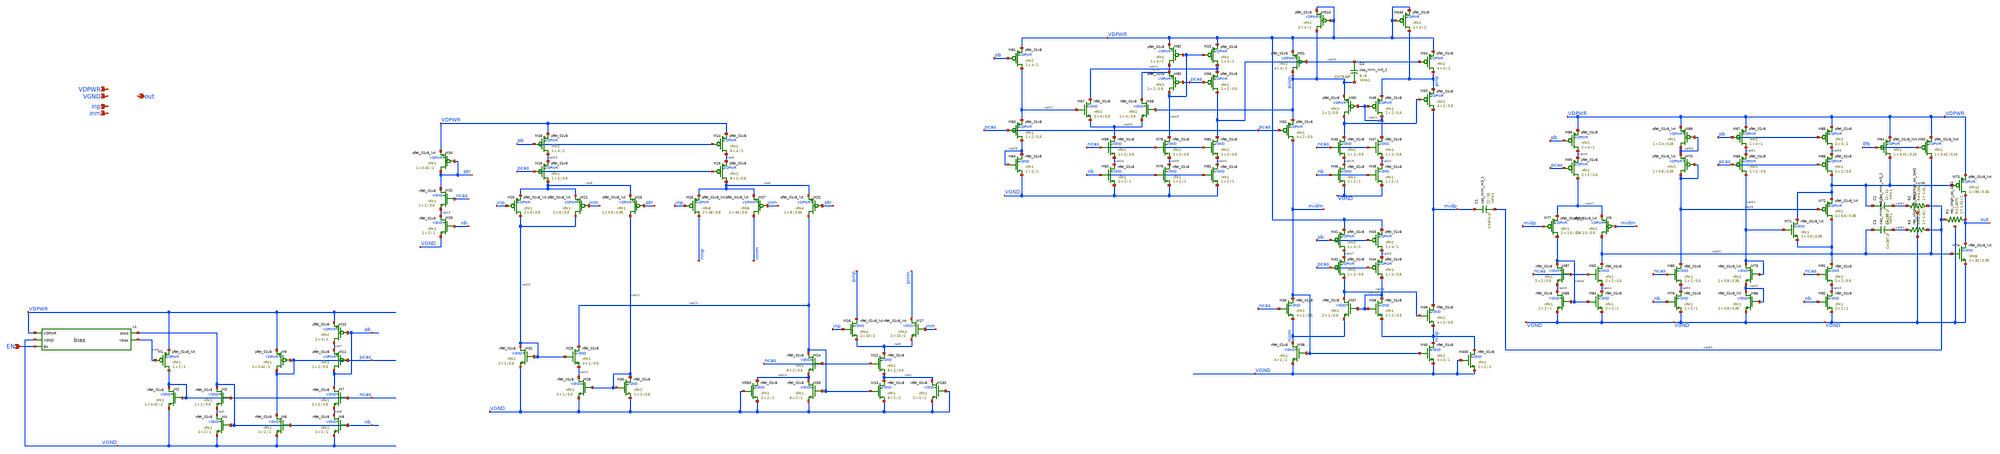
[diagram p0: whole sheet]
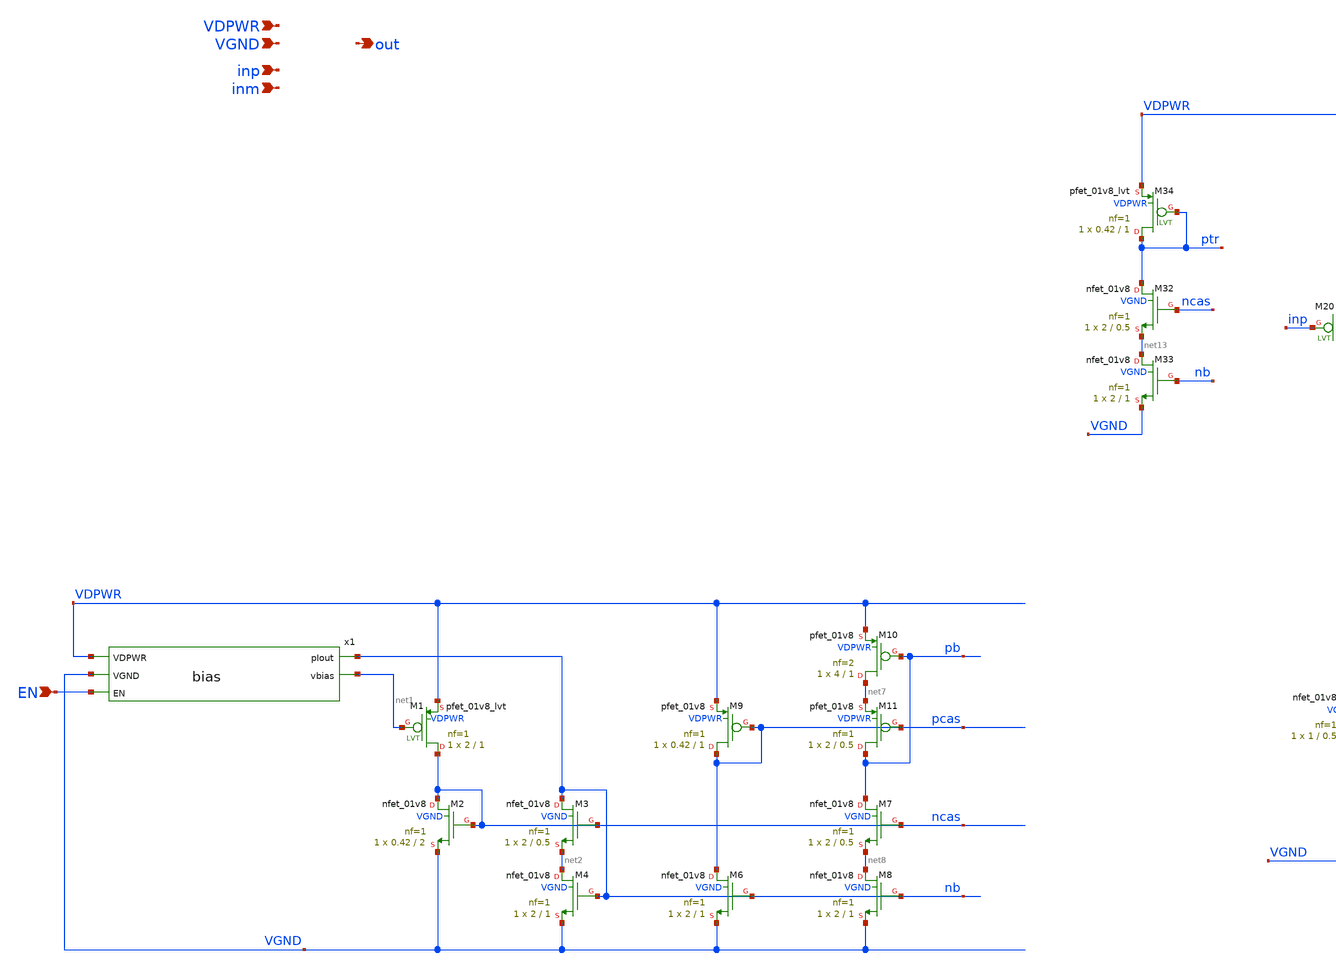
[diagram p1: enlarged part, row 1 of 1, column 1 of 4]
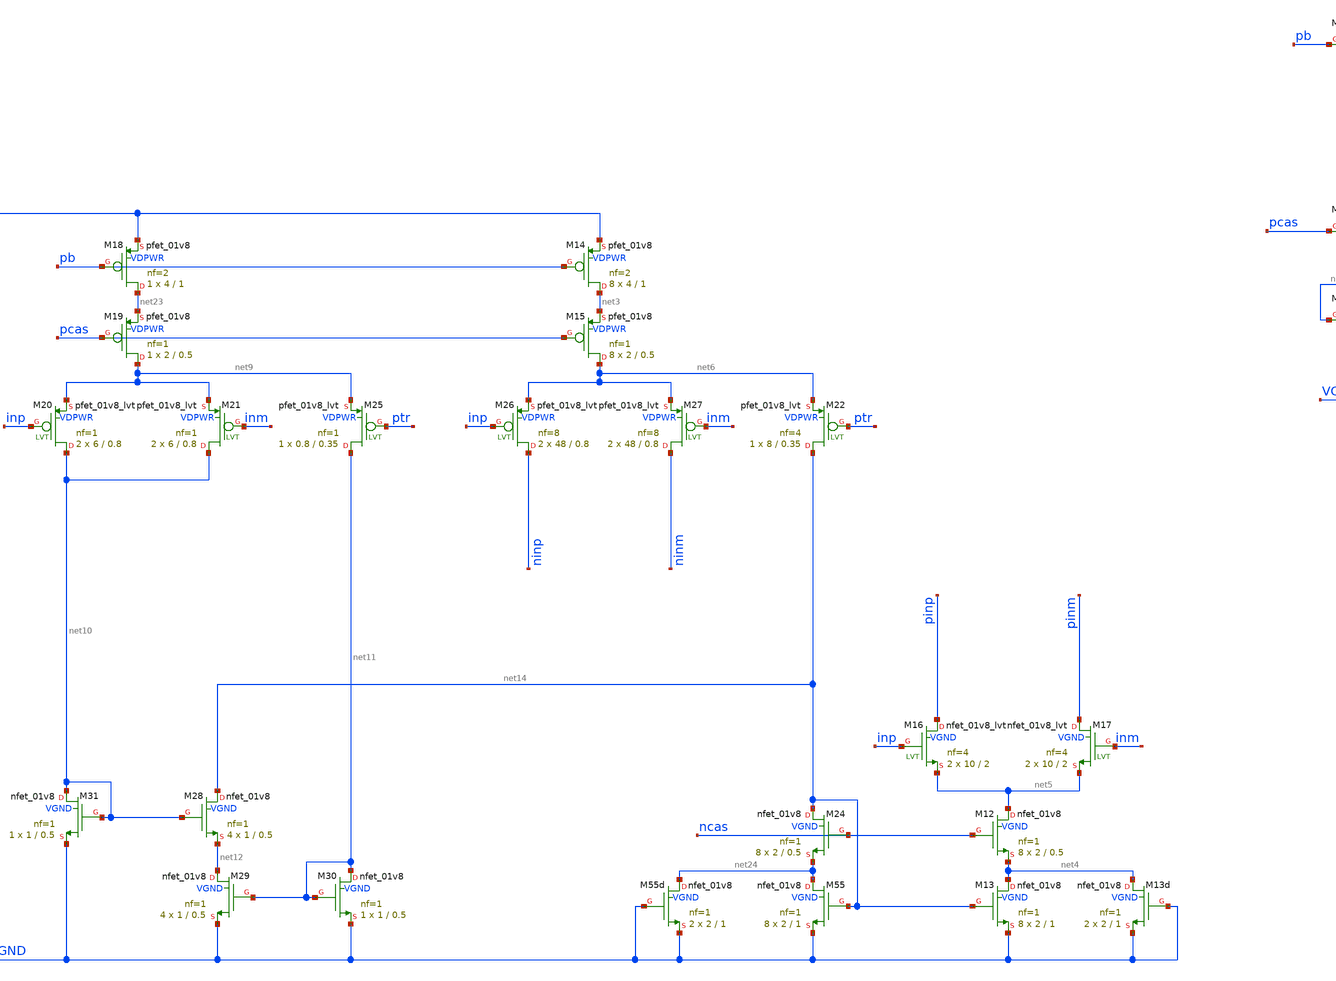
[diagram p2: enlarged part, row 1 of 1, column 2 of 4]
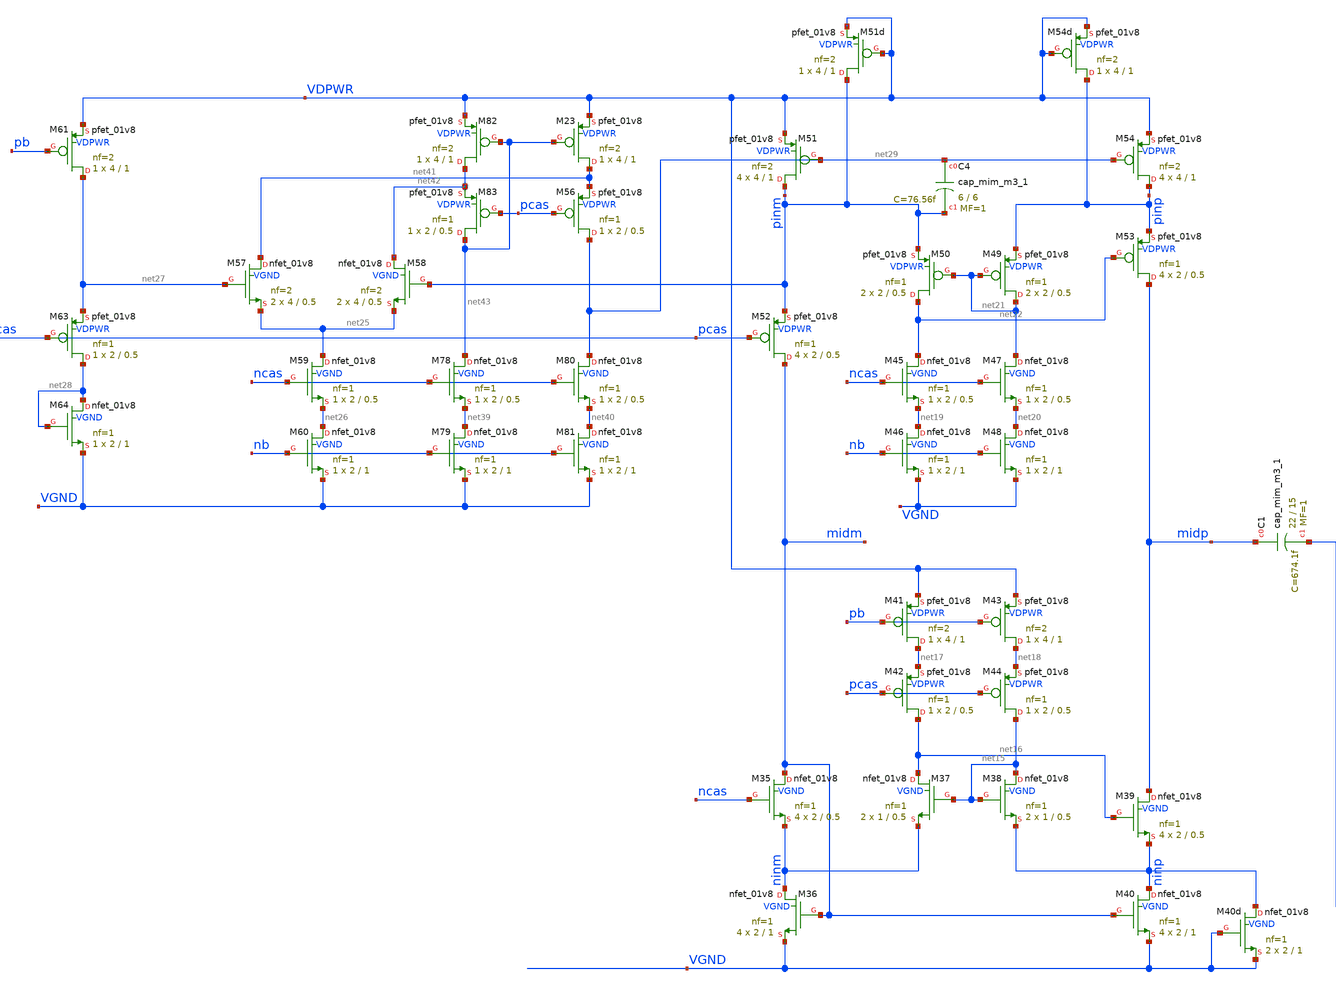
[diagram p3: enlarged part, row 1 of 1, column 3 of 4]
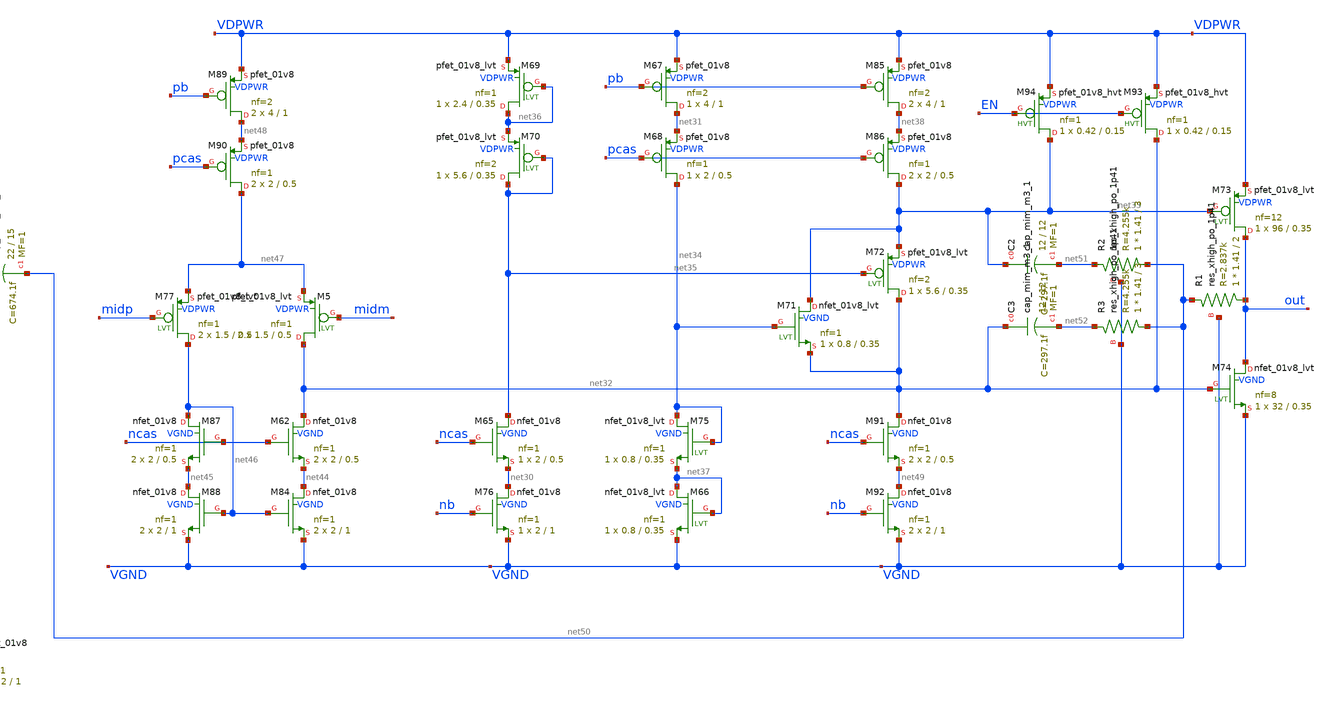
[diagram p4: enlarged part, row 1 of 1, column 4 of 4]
** sch_path: xschem/opamp.sch
**.subckt opamp VDPWR VGND inp inm out EN
*.ipin VDPWR
*.ipin VGND
*.ipin inp
*.ipin inm
*.opin out
*.ipin EN
x1 VDPWR nb VGND EN net1 bias
XM1 ncas net1 VDPWR VDPWR sky130_fd_pr__pfet_01v8_lvt L=1 W=2 nf=1 ad='int((1 + 1)/2) * 2 / 1 * 0.29'
+ as='int((1 + 2)/2) * 2 / 1 * 0.29' pd='2*int((1 + 1)/2) * (2 / 1 + 0.29)' ps='2*int((1 + 2)/2) * (2 / 1 + 0.29)'
+ nrd='0.29 / 2 ' nrs='0.29 / 2 ' sa=0 sb=0 sd=0 mult=1 m=1
XM2 ncas ncas VGND VGND sky130_fd_pr__nfet_01v8 L=2 W=0.42 nf=1 ad='int((1 + 1)/2) * 0.42 / 1 * 0.29'
+ as='int((1 + 2)/2) * 0.42 / 1 * 0.29' pd='2*int((1 + 1)/2) * (0.42 / 1 + 0.29)' ps='2*int((1 + 2)/2) * (0.42 / 1 + 0.29)'
+ nrd='0.29 / 0.42 ' nrs='0.29 / 0.42 ' sa=0 sb=0 sd=0 mult=1 m=1
XM3 nb ncas net2 VGND sky130_fd_pr__nfet_01v8 L=0.5 W=2 nf=1 ad='int((1 + 1)/2) * 2 / 1 * 0.29' as='int((1 + 2)/2) * 2 / 1 * 0.29'
+ pd='2*int((1 + 1)/2) * (2 / 1 + 0.29)' ps='2*int((1 + 2)/2) * (2 / 1 + 0.29)' nrd='0.29 / 2 ' nrs='0.29 / 2 '
+ sa=0 sb=0 sd=0 mult=1 m=1
XM4 net2 nb VGND VGND sky130_fd_pr__nfet_01v8 L=1 W=2 nf=1 ad='int((1 + 1)/2) * 2 / 1 * 0.29' as='int((1 + 2)/2) * 2 / 1 * 0.29'
+ pd='2*int((1 + 1)/2) * (2 / 1 + 0.29)' ps='2*int((1 + 2)/2) * (2 / 1 + 0.29)' nrd='0.29 / 2 ' nrs='0.29 / 2 '
+ sa=0 sb=0 sd=0 mult=1 m=1
XM6 pcas nb VGND VGND sky130_fd_pr__nfet_01v8 L=1 W=2 nf=1 ad='int((1 + 1)/2) * 2 / 1 * 0.29' as='int((1 + 2)/2) * 2 / 1 * 0.29'
+ pd='2*int((1 + 1)/2) * (2 / 1 + 0.29)' ps='2*int((1 + 2)/2) * (2 / 1 + 0.29)' nrd='0.29 / 2 ' nrs='0.29 / 2 '
+ sa=0 sb=0 sd=0 mult=1 m=1
XM7 pb ncas net8 VGND sky130_fd_pr__nfet_01v8 L=0.5 W=2 nf=1 ad='int((1 + 1)/2) * 2 / 1 * 0.29' as='int((1 + 2)/2) * 2 / 1 * 0.29'
+ pd='2*int((1 + 1)/2) * (2 / 1 + 0.29)' ps='2*int((1 + 2)/2) * (2 / 1 + 0.29)' nrd='0.29 / 2 ' nrs='0.29 / 2 '
+ sa=0 sb=0 sd=0 mult=1 m=1
XM8 net8 nb VGND VGND sky130_fd_pr__nfet_01v8 L=1 W=2 nf=1 ad='int((1 + 1)/2) * 2 / 1 * 0.29' as='int((1 + 2)/2) * 2 / 1 * 0.29'
+ pd='2*int((1 + 1)/2) * (2 / 1 + 0.29)' ps='2*int((1 + 2)/2) * (2 / 1 + 0.29)' nrd='0.29 / 2 ' nrs='0.29 / 2 '
+ sa=0 sb=0 sd=0 mult=1 m=1
XM9 pcas pcas VDPWR VDPWR sky130_fd_pr__pfet_01v8 L=1 W=0.42 nf=1 ad='int((1 + 1)/2) * 0.42 / 1 * 0.29'
+ as='int((1 + 2)/2) * 0.42 / 1 * 0.29' pd='2*int((1 + 1)/2) * (0.42 / 1 + 0.29)' ps='2*int((1 + 2)/2) * (0.42 / 1 + 0.29)'
+ nrd='0.29 / 0.42 ' nrs='0.29 / 0.42 ' sa=0 sb=0 sd=0 mult=1 m=1
XM10 net7 pb VDPWR VDPWR sky130_fd_pr__pfet_01v8 L=1 W=4 nf=2 ad='int((2 + 1)/2) * 4 / 2 * 0.29' as='int((2 + 2)/2) * 4 / 2 * 0.29'
+ pd='2*int((2 + 1)/2) * (4 / 2 + 0.29)' ps='2*int((2 + 2)/2) * (4 / 2 + 0.29)' nrd='0.29 / 4 ' nrs='0.29 / 4 '
+ sa=0 sb=0 sd=0 mult=1 m=1
XM11 pb pcas net7 VDPWR sky130_fd_pr__pfet_01v8 L=0.5 W=2 nf=1 ad='int((1 + 1)/2) * 2 / 1 * 0.29' as='int((1 + 2)/2) * 2 / 1 * 0.29'
+ pd='2*int((1 + 1)/2) * (2 / 1 + 0.29)' ps='2*int((1 + 2)/2) * (2 / 1 + 0.29)' nrd='0.29 / 2 ' nrs='0.29 / 2 '
+ sa=0 sb=0 sd=0 mult=1 m=1
XM12 net5 ncas net4 VGND sky130_fd_pr__nfet_01v8 L=0.5 W=2 nf=1 ad='int((1 + 1)/2) * 2 / 1 * 0.29' as='int((1 + 2)/2) * 2 / 1 * 0.29'
+ pd='2*int((1 + 1)/2) * (2 / 1 + 0.29)' ps='2*int((1 + 2)/2) * (2 / 1 + 0.29)' nrd='0.29 / 2 ' nrs='0.29 / 2 '
+ sa=0 sb=0 sd=0 mult=8 m=8
XM13 net4 net14 VGND VGND sky130_fd_pr__nfet_01v8 L=1 W=2 nf=1 ad='int((1 + 1)/2) * 2 / 1 * 0.29' as='int((1 + 2)/2) * 2 / 1 * 0.29'
+ pd='2*int((1 + 1)/2) * (2 / 1 + 0.29)' ps='2*int((1 + 2)/2) * (2 / 1 + 0.29)' nrd='0.29 / 2 ' nrs='0.29 / 2 '
+ sa=0 sb=0 sd=0 mult=8 m=8
XM14 net3 pb VDPWR VDPWR sky130_fd_pr__pfet_01v8 L=1 W=4 nf=2 ad='int((2 + 1)/2) * 4 / 2 * 0.29' as='int((2 + 2)/2) * 4 / 2 * 0.29'
+ pd='2*int((2 + 1)/2) * (4 / 2 + 0.29)' ps='2*int((2 + 2)/2) * (4 / 2 + 0.29)' nrd='0.29 / 4 ' nrs='0.29 / 4 '
+ sa=0 sb=0 sd=0 mult=8 m=8
XM15 net6 pcas net3 VDPWR sky130_fd_pr__pfet_01v8 L=0.5 W=2 nf=1 ad='int((1 + 1)/2) * 2 / 1 * 0.29' as='int((1 + 2)/2) * 2 / 1 * 0.29'
+ pd='2*int((1 + 1)/2) * (2 / 1 + 0.29)' ps='2*int((1 + 2)/2) * (2 / 1 + 0.29)' nrd='0.29 / 2 ' nrs='0.29 / 2 '
+ sa=0 sb=0 sd=0 mult=8 m=8
XM16 pinp inp net5 VGND sky130_fd_pr__nfet_01v8_lvt L=2 W=10 nf=4 ad='int((4 + 1)/2) * 10 / 4 * 0.29'
+ as='int((4 + 2)/2) * 10 / 4 * 0.29' pd='2*int((4 + 1)/2) * (10 / 4 + 0.29)' ps='2*int((4 + 2)/2) * (10 / 4 + 0.29)'
+ nrd='0.29 / 10 ' nrs='0.29 / 10 ' sa=0 sb=0 sd=0 mult=2 m=2
XM17 pinm inm net5 VGND sky130_fd_pr__nfet_01v8_lvt L=2 W=10 nf=4 ad='int((4 + 1)/2) * 10 / 4 * 0.29'
+ as='int((4 + 2)/2) * 10 / 4 * 0.29' pd='2*int((4 + 1)/2) * (10 / 4 + 0.29)' ps='2*int((4 + 2)/2) * (10 / 4 + 0.29)'
+ nrd='0.29 / 10 ' nrs='0.29 / 10 ' sa=0 sb=0 sd=0 mult=2 m=2
XM26 ninp inp net6 VDPWR sky130_fd_pr__pfet_01v8_lvt L=0.8 W=48 nf=8 ad='int((8 + 1)/2) * 48 / 8 * 0.29'
+ as='int((8 + 2)/2) * 48 / 8 * 0.29' pd='2*int((8 + 1)/2) * (48 / 8 + 0.29)' ps='2*int((8 + 2)/2) * (48 / 8 + 0.29)'
+ nrd='0.29 / 48 ' nrs='0.29 / 48 ' sa=0 sb=0 sd=0 mult=2 m=2
XM27 ninm inm net6 VDPWR sky130_fd_pr__pfet_01v8_lvt L=0.8 W=48 nf=8 ad='int((8 + 1)/2) * 48 / 8 * 0.29'
+ as='int((8 + 2)/2) * 48 / 8 * 0.29' pd='2*int((8 + 1)/2) * (48 / 8 + 0.29)' ps='2*int((8 + 2)/2) * (48 / 8 + 0.29)'
+ nrd='0.29 / 48 ' nrs='0.29 / 48 ' sa=0 sb=0 sd=0 mult=2 m=2
XM18 net23 pb VDPWR VDPWR sky130_fd_pr__pfet_01v8 L=1 W=4 nf=2 ad='int((2 + 1)/2) * 4 / 2 * 0.29' as='int((2 + 2)/2) * 4 / 2 * 0.29'
+ pd='2*int((2 + 1)/2) * (4 / 2 + 0.29)' ps='2*int((2 + 2)/2) * (4 / 2 + 0.29)' nrd='0.29 / 4 ' nrs='0.29 / 4 '
+ sa=0 sb=0 sd=0 mult=1 m=1
XM19 net9 pcas net23 VDPWR sky130_fd_pr__pfet_01v8 L=0.5 W=2 nf=1 ad='int((1 + 1)/2) * 2 / 1 * 0.29'
+ as='int((1 + 2)/2) * 2 / 1 * 0.29' pd='2*int((1 + 1)/2) * (2 / 1 + 0.29)' ps='2*int((1 + 2)/2) * (2 / 1 + 0.29)'
+ nrd='0.29 / 2 ' nrs='0.29 / 2 ' sa=0 sb=0 sd=0 mult=1 m=1
XM20 net10 inp net9 VDPWR sky130_fd_pr__pfet_01v8_lvt L=0.8 W=6 nf=1 ad='int((1 + 1)/2) * 6 / 1 * 0.29'
+ as='int((1 + 2)/2) * 6 / 1 * 0.29' pd='2*int((1 + 1)/2) * (6 / 1 + 0.29)' ps='2*int((1 + 2)/2) * (6 / 1 + 0.29)'
+ nrd='0.29 / 6 ' nrs='0.29 / 6 ' sa=0 sb=0 sd=0 mult=2 m=2
XM21 net10 inm net9 VDPWR sky130_fd_pr__pfet_01v8_lvt L=0.8 W=6 nf=1 ad='int((1 + 1)/2) * 6 / 1 * 0.29'
+ as='int((1 + 2)/2) * 6 / 1 * 0.29' pd='2*int((1 + 1)/2) * (6 / 1 + 0.29)' ps='2*int((1 + 2)/2) * (6 / 1 + 0.29)'
+ nrd='0.29 / 6 ' nrs='0.29 / 6 ' sa=0 sb=0 sd=0 mult=2 m=2
XM25 net11 ptr net9 VDPWR sky130_fd_pr__pfet_01v8_lvt L=0.35 W=0.8 nf=1 ad='int((1 + 1)/2) * 0.8 / 1 * 0.29'
+ as='int((1 + 2)/2) * 0.8 / 1 * 0.29' pd='2*int((1 + 1)/2) * (0.8 / 1 + 0.29)' ps='2*int((1 + 2)/2) * (0.8 / 1 + 0.29)'
+ nrd='0.29 / 0.8 ' nrs='0.29 / 0.8 ' sa=0 sb=0 sd=0 mult=1 m=1
XM28 net14 net10 net12 VGND sky130_fd_pr__nfet_01v8 L=0.5 W=1 nf=1 ad='int((1 + 1)/2) * 1 / 1 * 0.29'
+ as='int((1 + 2)/2) * 1 / 1 * 0.29' pd='2*int((1 + 1)/2) * (1 / 1 + 0.29)' ps='2*int((1 + 2)/2) * (1 / 1 + 0.29)'
+ nrd='0.29 / 1 ' nrs='0.29 / 1 ' sa=0 sb=0 sd=0 mult=4 m=4
XM29 net12 net11 VGND VGND sky130_fd_pr__nfet_01v8 L=0.5 W=1 nf=1 ad='int((1 + 1)/2) * 1 / 1 * 0.29'
+ as='int((1 + 2)/2) * 1 / 1 * 0.29' pd='2*int((1 + 1)/2) * (1 / 1 + 0.29)' ps='2*int((1 + 2)/2) * (1 / 1 + 0.29)'
+ nrd='0.29 / 1 ' nrs='0.29 / 1 ' sa=0 sb=0 sd=0 mult=4 m=4
XM30 net11 net11 VGND VGND sky130_fd_pr__nfet_01v8 L=0.5 W=1 nf=1 ad='int((1 + 1)/2) * 1 / 1 * 0.29'
+ as='int((1 + 2)/2) * 1 / 1 * 0.29' pd='2*int((1 + 1)/2) * (1 / 1 + 0.29)' ps='2*int((1 + 2)/2) * (1 / 1 + 0.29)'
+ nrd='0.29 / 1 ' nrs='0.29 / 1 ' sa=0 sb=0 sd=0 mult=1 m=1
XM31 net10 net10 VGND VGND sky130_fd_pr__nfet_01v8 L=0.5 W=1 nf=1 ad='int((1 + 1)/2) * 1 / 1 * 0.29'
+ as='int((1 + 2)/2) * 1 / 1 * 0.29' pd='2*int((1 + 1)/2) * (1 / 1 + 0.29)' ps='2*int((1 + 2)/2) * (1 / 1 + 0.29)'
+ nrd='0.29 / 1 ' nrs='0.29 / 1 ' sa=0 sb=0 sd=0 mult=1 m=1
XM32 ptr ncas net13 VGND sky130_fd_pr__nfet_01v8 L=0.5 W=2 nf=1 ad='int((1 + 1)/2) * 2 / 1 * 0.29' as='int((1 + 2)/2) * 2 / 1 * 0.29'
+ pd='2*int((1 + 1)/2) * (2 / 1 + 0.29)' ps='2*int((1 + 2)/2) * (2 / 1 + 0.29)' nrd='0.29 / 2 ' nrs='0.29 / 2 '
+ sa=0 sb=0 sd=0 mult=1 m=1
XM33 net13 nb VGND VGND sky130_fd_pr__nfet_01v8 L=1 W=2 nf=1 ad='int((1 + 1)/2) * 2 / 1 * 0.29' as='int((1 + 2)/2) * 2 / 1 * 0.29'
+ pd='2*int((1 + 1)/2) * (2 / 1 + 0.29)' ps='2*int((1 + 2)/2) * (2 / 1 + 0.29)' nrd='0.29 / 2 ' nrs='0.29 / 2 '
+ sa=0 sb=0 sd=0 mult=1 m=1
XM34 ptr ptr VDPWR VDPWR sky130_fd_pr__pfet_01v8_lvt L=1 W=0.42 nf=1 ad='int((1 + 1)/2) * 0.42 / 1 * 0.29'
+ as='int((1 + 2)/2) * 0.42 / 1 * 0.29' pd='2*int((1 + 1)/2) * (0.42 / 1 + 0.29)' ps='2*int((1 + 2)/2) * (0.42 / 1 + 0.29)'
+ nrd='0.29 / 0.42 ' nrs='0.29 / 0.42 ' sa=0 sb=0 sd=0 mult=1 m=1
XM35 midm ncas ninm VGND sky130_fd_pr__nfet_01v8 L=0.5 W=2 nf=1 ad='int((1 + 1)/2) * 2 / 1 * 0.29' as='int((1 + 2)/2) * 2 / 1 * 0.29'
+ pd='2*int((1 + 1)/2) * (2 / 1 + 0.29)' ps='2*int((1 + 2)/2) * (2 / 1 + 0.29)' nrd='0.29 / 2 ' nrs='0.29 / 2 '
+ sa=0 sb=0 sd=0 mult=4 m=4
XM36 ninm midm VGND VGND sky130_fd_pr__nfet_01v8 L=1 W=2 nf=1 ad='int((1 + 1)/2) * 2 / 1 * 0.29' as='int((1 + 2)/2) * 2 / 1 * 0.29'
+ pd='2*int((1 + 1)/2) * (2 / 1 + 0.29)' ps='2*int((1 + 2)/2) * (2 / 1 + 0.29)' nrd='0.29 / 2 ' nrs='0.29 / 2 '
+ sa=0 sb=0 sd=0 mult=4 m=4
XM37 net16 net15 ninm VGND sky130_fd_pr__nfet_01v8 L=0.5 W=1 nf=1 ad='int((1 + 1)/2) * 1 / 1 * 0.29'
+ as='int((1 + 2)/2) * 1 / 1 * 0.29' pd='2*int((1 + 1)/2) * (1 / 1 + 0.29)' ps='2*int((1 + 2)/2) * (1 / 1 + 0.29)'
+ nrd='0.29 / 1 ' nrs='0.29 / 1 ' sa=0 sb=0 sd=0 mult=2 m=2
XM39 midp net16 ninp VGND sky130_fd_pr__nfet_01v8 L=0.5 W=2 nf=1 ad='int((1 + 1)/2) * 2 / 1 * 0.29' as='int((1 + 2)/2) * 2 / 1 * 0.29'
+ pd='2*int((1 + 1)/2) * (2 / 1 + 0.29)' ps='2*int((1 + 2)/2) * (2 / 1 + 0.29)' nrd='0.29 / 2 ' nrs='0.29 / 2 '
+ sa=0 sb=0 sd=0 mult=4 m=4
XM40 ninp midm VGND VGND sky130_fd_pr__nfet_01v8 L=1 W=2 nf=1 ad='int((1 + 1)/2) * 2 / 1 * 0.29' as='int((1 + 2)/2) * 2 / 1 * 0.29'
+ pd='2*int((1 + 1)/2) * (2 / 1 + 0.29)' ps='2*int((1 + 2)/2) * (2 / 1 + 0.29)' nrd='0.29 / 2 ' nrs='0.29 / 2 '
+ sa=0 sb=0 sd=0 mult=4 m=4
XM41 net17 pb VDPWR VDPWR sky130_fd_pr__pfet_01v8 L=1 W=4 nf=2 ad='int((2 + 1)/2) * 4 / 2 * 0.29' as='int((2 + 2)/2) * 4 / 2 * 0.29'
+ pd='2*int((2 + 1)/2) * (4 / 2 + 0.29)' ps='2*int((2 + 2)/2) * (4 / 2 + 0.29)' nrd='0.29 / 4 ' nrs='0.29 / 4 '
+ sa=0 sb=0 sd=0 mult=1 m=1
XM42 net16 pcas net17 VDPWR sky130_fd_pr__pfet_01v8 L=0.5 W=2 nf=1 ad='int((1 + 1)/2) * 2 / 1 * 0.29'
+ as='int((1 + 2)/2) * 2 / 1 * 0.29' pd='2*int((1 + 1)/2) * (2 / 1 + 0.29)' ps='2*int((1 + 2)/2) * (2 / 1 + 0.29)'
+ nrd='0.29 / 2 ' nrs='0.29 / 2 ' sa=0 sb=0 sd=0 mult=1 m=1
XM43 net18 pb VDPWR VDPWR sky130_fd_pr__pfet_01v8 L=1 W=4 nf=2 ad='int((2 + 1)/2) * 4 / 2 * 0.29' as='int((2 + 2)/2) * 4 / 2 * 0.29'
+ pd='2*int((2 + 1)/2) * (4 / 2 + 0.29)' ps='2*int((2 + 2)/2) * (4 / 2 + 0.29)' nrd='0.29 / 4 ' nrs='0.29 / 4 '
+ sa=0 sb=0 sd=0 mult=1 m=1
XM44 net15 pcas net18 VDPWR sky130_fd_pr__pfet_01v8 L=0.5 W=2 nf=1 ad='int((1 + 1)/2) * 2 / 1 * 0.29'
+ as='int((1 + 2)/2) * 2 / 1 * 0.29' pd='2*int((1 + 1)/2) * (2 / 1 + 0.29)' ps='2*int((1 + 2)/2) * (2 / 1 + 0.29)'
+ nrd='0.29 / 2 ' nrs='0.29 / 2 ' sa=0 sb=0 sd=0 mult=1 m=1
XM45 net22 ncas net19 VGND sky130_fd_pr__nfet_01v8 L=0.5 W=2 nf=1 ad='int((1 + 1)/2) * 2 / 1 * 0.29'
+ as='int((1 + 2)/2) * 2 / 1 * 0.29' pd='2*int((1 + 1)/2) * (2 / 1 + 0.29)' ps='2*int((1 + 2)/2) * (2 / 1 + 0.29)'
+ nrd='0.29 / 2 ' nrs='0.29 / 2 ' sa=0 sb=0 sd=0 mult=1 m=1
XM46 net19 nb VGND VGND sky130_fd_pr__nfet_01v8 L=1 W=2 nf=1 ad='int((1 + 1)/2) * 2 / 1 * 0.29' as='int((1 + 2)/2) * 2 / 1 * 0.29'
+ pd='2*int((1 + 1)/2) * (2 / 1 + 0.29)' ps='2*int((1 + 2)/2) * (2 / 1 + 0.29)' nrd='0.29 / 2 ' nrs='0.29 / 2 '
+ sa=0 sb=0 sd=0 mult=1 m=1
XM47 net21 ncas net20 VGND sky130_fd_pr__nfet_01v8 L=0.5 W=2 nf=1 ad='int((1 + 1)/2) * 2 / 1 * 0.29'
+ as='int((1 + 2)/2) * 2 / 1 * 0.29' pd='2*int((1 + 1)/2) * (2 / 1 + 0.29)' ps='2*int((1 + 2)/2) * (2 / 1 + 0.29)'
+ nrd='0.29 / 2 ' nrs='0.29 / 2 ' sa=0 sb=0 sd=0 mult=1 m=1
XM48 net20 nb VGND VGND sky130_fd_pr__nfet_01v8 L=1 W=2 nf=1 ad='int((1 + 1)/2) * 2 / 1 * 0.29' as='int((1 + 2)/2) * 2 / 1 * 0.29'
+ pd='2*int((1 + 1)/2) * (2 / 1 + 0.29)' ps='2*int((1 + 2)/2) * (2 / 1 + 0.29)' nrd='0.29 / 2 ' nrs='0.29 / 2 '
+ sa=0 sb=0 sd=0 mult=1 m=1
XM50 net22 net21 pinm VDPWR sky130_fd_pr__pfet_01v8 L=0.5 W=2 nf=1 ad='int((1 + 1)/2) * 2 / 1 * 0.29'
+ as='int((1 + 2)/2) * 2 / 1 * 0.29' pd='2*int((1 + 1)/2) * (2 / 1 + 0.29)' ps='2*int((1 + 2)/2) * (2 / 1 + 0.29)'
+ nrd='0.29 / 2 ' nrs='0.29 / 2 ' sa=0 sb=0 sd=0 mult=2 m=2
XM51 pinm net29 VDPWR VDPWR sky130_fd_pr__pfet_01v8 L=1 W=4 nf=2 ad='int((2 + 1)/2) * 4 / 2 * 0.29' as='int((2 + 2)/2) * 4 / 2 * 0.29'
+ pd='2*int((2 + 1)/2) * (4 / 2 + 0.29)' ps='2*int((2 + 2)/2) * (4 / 2 + 0.29)' nrd='0.29 / 4 ' nrs='0.29 / 4 '
+ sa=0 sb=0 sd=0 mult=4 m=4
XM52 midm pcas pinm VDPWR sky130_fd_pr__pfet_01v8 L=0.5 W=2 nf=1 ad='int((1 + 1)/2) * 2 / 1 * 0.29' as='int((1 + 2)/2) * 2 / 1 * 0.29'
+ pd='2*int((1 + 1)/2) * (2 / 1 + 0.29)' ps='2*int((1 + 2)/2) * (2 / 1 + 0.29)' nrd='0.29 / 2 ' nrs='0.29 / 2 '
+ sa=0 sb=0 sd=0 mult=4 m=4
XM53 midp net22 pinp VDPWR sky130_fd_pr__pfet_01v8 L=0.5 W=2 nf=1 ad='int((1 + 1)/2) * 2 / 1 * 0.29'
+ as='int((1 + 2)/2) * 2 / 1 * 0.29' pd='2*int((1 + 1)/2) * (2 / 1 + 0.29)' ps='2*int((1 + 2)/2) * (2 / 1 + 0.29)'
+ nrd='0.29 / 2 ' nrs='0.29 / 2 ' sa=0 sb=0 sd=0 mult=4 m=4
XM54 pinp net29 VDPWR VDPWR sky130_fd_pr__pfet_01v8 L=1 W=4 nf=2 ad='int((2 + 1)/2) * 4 / 2 * 0.29' as='int((2 + 2)/2) * 4 / 2 * 0.29'
+ pd='2*int((2 + 1)/2) * (4 / 2 + 0.29)' ps='2*int((2 + 2)/2) * (4 / 2 + 0.29)' nrd='0.29 / 4 ' nrs='0.29 / 4 '
+ sa=0 sb=0 sd=0 mult=4 m=4
XM49 net21 net21 pinp VDPWR sky130_fd_pr__pfet_01v8 L=0.5 W=2 nf=1 ad='int((1 + 1)/2) * 2 / 1 * 0.29'
+ as='int((1 + 2)/2) * 2 / 1 * 0.29' pd='2*int((1 + 1)/2) * (2 / 1 + 0.29)' ps='2*int((1 + 2)/2) * (2 / 1 + 0.29)'
+ nrd='0.29 / 2 ' nrs='0.29 / 2 ' sa=0 sb=0 sd=0 mult=2 m=2
XM38 net15 net15 ninp VGND sky130_fd_pr__nfet_01v8 L=0.5 W=1 nf=1 ad='int((1 + 1)/2) * 1 / 1 * 0.29'
+ as='int((1 + 2)/2) * 1 / 1 * 0.29' pd='2*int((1 + 1)/2) * (1 / 1 + 0.29)' ps='2*int((1 + 2)/2) * (1 / 1 + 0.29)'
+ nrd='0.29 / 1 ' nrs='0.29 / 1 ' sa=0 sb=0 sd=0 mult=2 m=2
XM24 net14 ncas net24 VGND sky130_fd_pr__nfet_01v8 L=0.5 W=2 nf=1 ad='int((1 + 1)/2) * 2 / 1 * 0.29'
+ as='int((1 + 2)/2) * 2 / 1 * 0.29' pd='2*int((1 + 1)/2) * (2 / 1 + 0.29)' ps='2*int((1 + 2)/2) * (2 / 1 + 0.29)'
+ nrd='0.29 / 2 ' nrs='0.29 / 2 ' sa=0 sb=0 sd=0 mult=8 m=8
XM55 net24 net14 VGND VGND sky130_fd_pr__nfet_01v8 L=1 W=2 nf=1 ad='int((1 + 1)/2) * 2 / 1 * 0.29' as='int((1 + 2)/2) * 2 / 1 * 0.29'
+ pd='2*int((1 + 1)/2) * (2 / 1 + 0.29)' ps='2*int((1 + 2)/2) * (2 / 1 + 0.29)' nrd='0.29 / 2 ' nrs='0.29 / 2 '
+ sa=0 sb=0 sd=0 mult=8 m=8
XM22 net14 ptr net6 VDPWR sky130_fd_pr__pfet_01v8_lvt L=0.35 W=8 nf=4 ad='int((4 + 1)/2) * 8 / 4 * 0.29'
+ as='int((4 + 2)/2) * 8 / 4 * 0.29' pd='2*int((4 + 1)/2) * (8 / 4 + 0.29)' ps='2*int((4 + 2)/2) * (8 / 4 + 0.29)'
+ nrd='0.29 / 8 ' nrs='0.29 / 8 ' sa=0 sb=0 sd=0 mult=1 m=1
XM57 net41 net27 net25 VGND sky130_fd_pr__nfet_01v8 L=0.5 W=4 nf=2 ad='int((2 + 1)/2) * 4 / 2 * 0.29'
+ as='int((2 + 2)/2) * 4 / 2 * 0.29' pd='2*int((2 + 1)/2) * (4 / 2 + 0.29)' ps='2*int((2 + 2)/2) * (4 / 2 + 0.29)'
+ nrd='0.29 / 4 ' nrs='0.29 / 4 ' sa=0 sb=0 sd=0 mult=2 m=2
XM58 net42 pinm net25 VGND sky130_fd_pr__nfet_01v8 L=0.5 W=4 nf=2 ad='int((2 + 1)/2) * 4 / 2 * 0.29'
+ as='int((2 + 2)/2) * 4 / 2 * 0.29' pd='2*int((2 + 1)/2) * (4 / 2 + 0.29)' ps='2*int((2 + 2)/2) * (4 / 2 + 0.29)'
+ nrd='0.29 / 4 ' nrs='0.29 / 4 ' sa=0 sb=0 sd=0 mult=2 m=2
XM59 net25 ncas net26 VGND sky130_fd_pr__nfet_01v8 L=0.5 W=2 nf=1 ad='int((1 + 1)/2) * 2 / 1 * 0.29'
+ as='int((1 + 2)/2) * 2 / 1 * 0.29' pd='2*int((1 + 1)/2) * (2 / 1 + 0.29)' ps='2*int((1 + 2)/2) * (2 / 1 + 0.29)'
+ nrd='0.29 / 2 ' nrs='0.29 / 2 ' sa=0 sb=0 sd=0 mult=1 m=1
XM60 net26 nb VGND VGND sky130_fd_pr__nfet_01v8 L=1 W=2 nf=1 ad='int((1 + 1)/2) * 2 / 1 * 0.29' as='int((1 + 2)/2) * 2 / 1 * 0.29'
+ pd='2*int((1 + 1)/2) * (2 / 1 + 0.29)' ps='2*int((1 + 2)/2) * (2 / 1 + 0.29)' nrd='0.29 / 2 ' nrs='0.29 / 2 '
+ sa=0 sb=0 sd=0 mult=1 m=1
XM61 net27 pb VDPWR VDPWR sky130_fd_pr__pfet_01v8 L=1 W=4 nf=2 ad='int((2 + 1)/2) * 4 / 2 * 0.29' as='int((2 + 2)/2) * 4 / 2 * 0.29'
+ pd='2*int((2 + 1)/2) * (4 / 2 + 0.29)' ps='2*int((2 + 2)/2) * (4 / 2 + 0.29)' nrd='0.29 / 4 ' nrs='0.29 / 4 '
+ sa=0 sb=0 sd=0 mult=1 m=1
XM63 net28 pcas net27 VDPWR sky130_fd_pr__pfet_01v8 L=0.5 W=2 nf=1 ad='int((1 + 1)/2) * 2 / 1 * 0.29'
+ as='int((1 + 2)/2) * 2 / 1 * 0.29' pd='2*int((1 + 1)/2) * (2 / 1 + 0.29)' ps='2*int((1 + 2)/2) * (2 / 1 + 0.29)'
+ nrd='0.29 / 2 ' nrs='0.29 / 2 ' sa=0 sb=0 sd=0 mult=1 m=1
XM64 net28 net28 VGND VGND sky130_fd_pr__nfet_01v8 L=1 W=2 nf=1 ad='int((1 + 1)/2) * 2 / 1 * 0.29' as='int((1 + 2)/2) * 2 / 1 * 0.29'
+ pd='2*int((1 + 1)/2) * (2 / 1 + 0.29)' ps='2*int((1 + 2)/2) * (2 / 1 + 0.29)' nrd='0.29 / 2 ' nrs='0.29 / 2 '
+ sa=0 sb=0 sd=0 mult=1 m=1
XM65 net35 ncas net30 VGND sky130_fd_pr__nfet_01v8 L=0.5 W=2 nf=1 ad='int((1 + 1)/2) * 2 / 1 * 0.29'
+ as='int((1 + 2)/2) * 2 / 1 * 0.29' pd='2*int((1 + 1)/2) * (2 / 1 + 0.29)' ps='2*int((1 + 2)/2) * (2 / 1 + 0.29)'
+ nrd='0.29 / 2 ' nrs='0.29 / 2 ' sa=0 sb=0 sd=0 mult=1 m=1
XM66 net37 net37 VGND VGND sky130_fd_pr__nfet_01v8_lvt L=0.35 W=0.8 nf=1 ad='int((1 + 1)/2) * 0.8 / 1 * 0.29'
+ as='int((1 + 2)/2) * 0.8 / 1 * 0.29' pd='2*int((1 + 1)/2) * (0.8 / 1 + 0.29)' ps='2*int((1 + 2)/2) * (0.8 / 1 + 0.29)'
+ nrd='0.29 / 0.8 ' nrs='0.29 / 0.8 ' sa=0 sb=0 sd=0 mult=1 m=1
XM67 net31 pb VDPWR VDPWR sky130_fd_pr__pfet_01v8 L=1 W=4 nf=2 ad='int((2 + 1)/2) * 4 / 2 * 0.29' as='int((2 + 2)/2) * 4 / 2 * 0.29'
+ pd='2*int((2 + 1)/2) * (4 / 2 + 0.29)' ps='2*int((2 + 2)/2) * (4 / 2 + 0.29)' nrd='0.29 / 4 ' nrs='0.29 / 4 '
+ sa=0 sb=0 sd=0 mult=1 m=1
XM68 net34 pcas net31 VDPWR sky130_fd_pr__pfet_01v8 L=0.5 W=2 nf=1 ad='int((1 + 1)/2) * 2 / 1 * 0.29'
+ as='int((1 + 2)/2) * 2 / 1 * 0.29' pd='2*int((1 + 1)/2) * (2 / 1 + 0.29)' ps='2*int((1 + 2)/2) * (2 / 1 + 0.29)'
+ nrd='0.29 / 2 ' nrs='0.29 / 2 ' sa=0 sb=0 sd=0 mult=1 m=1
XM69 net36 net36 VDPWR VDPWR sky130_fd_pr__pfet_01v8_lvt L=0.35 W=2.4 nf=1 ad='int((1 + 1)/2) * 2.4 / 1 * 0.29'
+ as='int((1 + 2)/2) * 2.4 / 1 * 0.29' pd='2*int((1 + 1)/2) * (2.4 / 1 + 0.29)' ps='2*int((1 + 2)/2) * (2.4 / 1 + 0.29)'
+ nrd='0.29 / 2.4 ' nrs='0.29 / 2.4 ' sa=0 sb=0 sd=0 mult=1 m=1
XM70 net35 net35 net36 VDPWR sky130_fd_pr__pfet_01v8_lvt L=0.35 W=5.6 nf=2 ad='int((2 + 1)/2) * 5.6 / 2 * 0.29'
+ as='int((2 + 2)/2) * 5.6 / 2 * 0.29' pd='2*int((2 + 1)/2) * (5.6 / 2 + 0.29)' ps='2*int((2 + 2)/2) * (5.6 / 2 + 0.29)'
+ nrd='0.29 / 5.6 ' nrs='0.29 / 5.6 ' sa=0 sb=0 sd=0 mult=1 m=1
XM71 net33 net34 net32 VGND sky130_fd_pr__nfet_01v8_lvt L=0.35 W=0.8 nf=1 ad='int((1 + 1)/2) * 0.8 / 1 * 0.29'
+ as='int((1 + 2)/2) * 0.8 / 1 * 0.29' pd='2*int((1 + 1)/2) * (0.8 / 1 + 0.29)' ps='2*int((1 + 2)/2) * (0.8 / 1 + 0.29)'
+ nrd='0.29 / 0.8 ' nrs='0.29 / 0.8 ' sa=0 sb=0 sd=0 mult=1 m=1
XM72 net32 net35 net33 VDPWR sky130_fd_pr__pfet_01v8_lvt L=0.35 W=5.6 nf=2 ad='int((2 + 1)/2) * 5.6 / 2 * 0.29'
+ as='int((2 + 2)/2) * 5.6 / 2 * 0.29' pd='2*int((2 + 1)/2) * (5.6 / 2 + 0.29)' ps='2*int((2 + 2)/2) * (5.6 / 2 + 0.29)'
+ nrd='0.29 / 5.6 ' nrs='0.29 / 5.6 ' sa=0 sb=0 sd=0 mult=1 m=1
XM73 out net33 VDPWR VDPWR sky130_fd_pr__pfet_01v8_lvt L=0.35 W=96 nf=12 ad='int((12 + 1)/2) * 96 / 12 * 0.29'
+ as='int((12 + 2)/2) * 96 / 12 * 0.29' pd='2*int((12 + 1)/2) * (96 / 12 + 0.29)' ps='2*int((12 + 2)/2) * (96 / 12 + 0.29)'
+ nrd='0.29 / 96 ' nrs='0.29 / 96 ' sa=0 sb=0 sd=0 mult=1 m=1
XM74 out net32 VGND VGND sky130_fd_pr__nfet_01v8_lvt L=0.35 W=32 nf=8 ad='int((8 + 1)/2) * 32 / 8 * 0.29'
+ as='int((8 + 2)/2) * 32 / 8 * 0.29' pd='2*int((8 + 1)/2) * (32 / 8 + 0.29)' ps='2*int((8 + 2)/2) * (32 / 8 + 0.29)'
+ nrd='0.29 / 32 ' nrs='0.29 / 32 ' sa=0 sb=0 sd=0 mult=1 m=1
XM75 net34 net34 net37 VGND sky130_fd_pr__nfet_01v8_lvt L=0.35 W=0.8 nf=1 ad='int((1 + 1)/2) * 0.8 / 1 * 0.29'
+ as='int((1 + 2)/2) * 0.8 / 1 * 0.29' pd='2*int((1 + 1)/2) * (0.8 / 1 + 0.29)' ps='2*int((1 + 2)/2) * (0.8 / 1 + 0.29)'
+ nrd='0.29 / 0.8 ' nrs='0.29 / 0.8 ' sa=0 sb=0 sd=0 mult=1 m=1
XM76 net30 nb VGND VGND sky130_fd_pr__nfet_01v8 L=1 W=2 nf=1 ad='int((1 + 1)/2) * 2 / 1 * 0.29' as='int((1 + 2)/2) * 2 / 1 * 0.29'
+ pd='2*int((1 + 1)/2) * (2 / 1 + 0.29)' ps='2*int((1 + 2)/2) * (2 / 1 + 0.29)' nrd='0.29 / 2 ' nrs='0.29 / 2 '
+ sa=0 sb=0 sd=0 mult=1 m=1
XM85 net38 pb VDPWR VDPWR sky130_fd_pr__pfet_01v8 L=1 W=4 nf=2 ad='int((2 + 1)/2) * 4 / 2 * 0.29' as='int((2 + 2)/2) * 4 / 2 * 0.29'
+ pd='2*int((2 + 1)/2) * (4 / 2 + 0.29)' ps='2*int((2 + 2)/2) * (4 / 2 + 0.29)' nrd='0.29 / 4 ' nrs='0.29 / 4 '
+ sa=0 sb=0 sd=0 mult=2 m=2
XM86 net33 pcas net38 VDPWR sky130_fd_pr__pfet_01v8 L=0.5 W=2 nf=1 ad='int((1 + 1)/2) * 2 / 1 * 0.29'
+ as='int((1 + 2)/2) * 2 / 1 * 0.29' pd='2*int((1 + 1)/2) * (2 / 1 + 0.29)' ps='2*int((1 + 2)/2) * (2 / 1 + 0.29)'
+ nrd='0.29 / 2 ' nrs='0.29 / 2 ' sa=0 sb=0 sd=0 mult=2 m=2
XM77 net46 midp net47 VDPWR sky130_fd_pr__pfet_01v8_lvt L=0.5 W=1.5 nf=1 ad='int((1 + 1)/2) * 1.5 / 1 * 0.29'
+ as='int((1 + 2)/2) * 1.5 / 1 * 0.29' pd='2*int((1 + 1)/2) * (1.5 / 1 + 0.29)' ps='2*int((1 + 2)/2) * (1.5 / 1 + 0.29)'
+ nrd='0.29 / 1.5 ' nrs='0.29 / 1.5 ' sa=0 sb=0 sd=0 mult=2 m=2
XM78 net43 ncas net39 VGND sky130_fd_pr__nfet_01v8 L=0.5 W=2 nf=1 ad='int((1 + 1)/2) * 2 / 1 * 0.29'
+ as='int((1 + 2)/2) * 2 / 1 * 0.29' pd='2*int((1 + 1)/2) * (2 / 1 + 0.29)' ps='2*int((1 + 2)/2) * (2 / 1 + 0.29)'
+ nrd='0.29 / 2 ' nrs='0.29 / 2 ' sa=0 sb=0 sd=0 mult=1 m=1
XM79 net39 nb VGND VGND sky130_fd_pr__nfet_01v8 L=1 W=2 nf=1 ad='int((1 + 1)/2) * 2 / 1 * 0.29' as='int((1 + 2)/2) * 2 / 1 * 0.29'
+ pd='2*int((1 + 1)/2) * (2 / 1 + 0.29)' ps='2*int((1 + 2)/2) * (2 / 1 + 0.29)' nrd='0.29 / 2 ' nrs='0.29 / 2 '
+ sa=0 sb=0 sd=0 mult=1 m=1
XM80 net29 ncas net40 VGND sky130_fd_pr__nfet_01v8 L=0.5 W=2 nf=1 ad='int((1 + 1)/2) * 2 / 1 * 0.29'
+ as='int((1 + 2)/2) * 2 / 1 * 0.29' pd='2*int((1 + 1)/2) * (2 / 1 + 0.29)' ps='2*int((1 + 2)/2) * (2 / 1 + 0.29)'
+ nrd='0.29 / 2 ' nrs='0.29 / 2 ' sa=0 sb=0 sd=0 mult=1 m=1
XM81 net40 nb VGND VGND sky130_fd_pr__nfet_01v8 L=1 W=2 nf=1 ad='int((1 + 1)/2) * 2 / 1 * 0.29' as='int((1 + 2)/2) * 2 / 1 * 0.29'
+ pd='2*int((1 + 1)/2) * (2 / 1 + 0.29)' ps='2*int((1 + 2)/2) * (2 / 1 + 0.29)' nrd='0.29 / 2 ' nrs='0.29 / 2 '
+ sa=0 sb=0 sd=0 mult=1 m=1
XM23 net41 net43 VDPWR VDPWR sky130_fd_pr__pfet_01v8 L=1 W=4 nf=2 ad='int((2 + 1)/2) * 4 / 2 * 0.29'
+ as='int((2 + 2)/2) * 4 / 2 * 0.29' pd='2*int((2 + 1)/2) * (4 / 2 + 0.29)' ps='2*int((2 + 2)/2) * (4 / 2 + 0.29)'
+ nrd='0.29 / 4 ' nrs='0.29 / 4 ' sa=0 sb=0 sd=0 mult=1 m=1
XM56 net29 pcas net41 VDPWR sky130_fd_pr__pfet_01v8 L=0.5 W=2 nf=1 ad='int((1 + 1)/2) * 2 / 1 * 0.29'
+ as='int((1 + 2)/2) * 2 / 1 * 0.29' pd='2*int((1 + 1)/2) * (2 / 1 + 0.29)' ps='2*int((1 + 2)/2) * (2 / 1 + 0.29)'
+ nrd='0.29 / 2 ' nrs='0.29 / 2 ' sa=0 sb=0 sd=0 mult=1 m=1
XM82 net42 net43 VDPWR VDPWR sky130_fd_pr__pfet_01v8 L=1 W=4 nf=2 ad='int((2 + 1)/2) * 4 / 2 * 0.29'
+ as='int((2 + 2)/2) * 4 / 2 * 0.29' pd='2*int((2 + 1)/2) * (4 / 2 + 0.29)' ps='2*int((2 + 2)/2) * (4 / 2 + 0.29)'
+ nrd='0.29 / 4 ' nrs='0.29 / 4 ' sa=0 sb=0 sd=0 mult=1 m=1
XM83 net43 pcas net42 VDPWR sky130_fd_pr__pfet_01v8 L=0.5 W=2 nf=1 ad='int((1 + 1)/2) * 2 / 1 * 0.29'
+ as='int((1 + 2)/2) * 2 / 1 * 0.29' pd='2*int((1 + 1)/2) * (2 / 1 + 0.29)' ps='2*int((1 + 2)/2) * (2 / 1 + 0.29)'
+ nrd='0.29 / 2 ' nrs='0.29 / 2 ' sa=0 sb=0 sd=0 mult=1 m=1
XC4 net29 pinm sky130_fd_pr__cap_mim_m3_1 W=6 L=6 MF=1 m=1
XM5 net32 midm net47 VDPWR sky130_fd_pr__pfet_01v8_lvt L=0.5 W=1.5 nf=1 ad='int((1 + 1)/2) * 1.5 / 1 * 0.29'
+ as='int((1 + 2)/2) * 1.5 / 1 * 0.29' pd='2*int((1 + 1)/2) * (1.5 / 1 + 0.29)' ps='2*int((1 + 2)/2) * (1.5 / 1 + 0.29)'
+ nrd='0.29 / 1.5 ' nrs='0.29 / 1.5 ' sa=0 sb=0 sd=0 mult=2 m=2
XM62 net32 ncas net44 VGND sky130_fd_pr__nfet_01v8 L=0.5 W=2 nf=1 ad='int((1 + 1)/2) * 2 / 1 * 0.29'
+ as='int((1 + 2)/2) * 2 / 1 * 0.29' pd='2*int((1 + 1)/2) * (2 / 1 + 0.29)' ps='2*int((1 + 2)/2) * (2 / 1 + 0.29)'
+ nrd='0.29 / 2 ' nrs='0.29 / 2 ' sa=0 sb=0 sd=0 mult=2 m=2
XM84 net44 net46 VGND VGND sky130_fd_pr__nfet_01v8 L=1 W=2 nf=1 ad='int((1 + 1)/2) * 2 / 1 * 0.29' as='int((1 + 2)/2) * 2 / 1 * 0.29'
+ pd='2*int((1 + 1)/2) * (2 / 1 + 0.29)' ps='2*int((1 + 2)/2) * (2 / 1 + 0.29)' nrd='0.29 / 2 ' nrs='0.29 / 2 '
+ sa=0 sb=0 sd=0 mult=2 m=2
XM87 net46 ncas net45 VGND sky130_fd_pr__nfet_01v8 L=0.5 W=2 nf=1 ad='int((1 + 1)/2) * 2 / 1 * 0.29'
+ as='int((1 + 2)/2) * 2 / 1 * 0.29' pd='2*int((1 + 1)/2) * (2 / 1 + 0.29)' ps='2*int((1 + 2)/2) * (2 / 1 + 0.29)'
+ nrd='0.29 / 2 ' nrs='0.29 / 2 ' sa=0 sb=0 sd=0 mult=2 m=2
XM88 net45 net46 VGND VGND sky130_fd_pr__nfet_01v8 L=1 W=2 nf=1 ad='int((1 + 1)/2) * 2 / 1 * 0.29' as='int((1 + 2)/2) * 2 / 1 * 0.29'
+ pd='2*int((1 + 1)/2) * (2 / 1 + 0.29)' ps='2*int((1 + 2)/2) * (2 / 1 + 0.29)' nrd='0.29 / 2 ' nrs='0.29 / 2 '
+ sa=0 sb=0 sd=0 mult=2 m=2
XM89 net48 pb VDPWR VDPWR sky130_fd_pr__pfet_01v8 L=1 W=4 nf=2 ad='int((2 + 1)/2) * 4 / 2 * 0.29' as='int((2 + 2)/2) * 4 / 2 * 0.29'
+ pd='2*int((2 + 1)/2) * (4 / 2 + 0.29)' ps='2*int((2 + 2)/2) * (4 / 2 + 0.29)' nrd='0.29 / 4 ' nrs='0.29 / 4 '
+ sa=0 sb=0 sd=0 mult=2 m=2
XM90 net47 pcas net48 VDPWR sky130_fd_pr__pfet_01v8 L=0.5 W=2 nf=1 ad='int((1 + 1)/2) * 2 / 1 * 0.29'
+ as='int((1 + 2)/2) * 2 / 1 * 0.29' pd='2*int((1 + 1)/2) * (2 / 1 + 0.29)' ps='2*int((1 + 2)/2) * (2 / 1 + 0.29)'
+ nrd='0.29 / 2 ' nrs='0.29 / 2 ' sa=0 sb=0 sd=0 mult=2 m=2
XM91 net32 ncas net49 VGND sky130_fd_pr__nfet_01v8 L=0.5 W=2 nf=1 ad='int((1 + 1)/2) * 2 / 1 * 0.29'
+ as='int((1 + 2)/2) * 2 / 1 * 0.29' pd='2*int((1 + 1)/2) * (2 / 1 + 0.29)' ps='2*int((1 + 2)/2) * (2 / 1 + 0.29)'
+ nrd='0.29 / 2 ' nrs='0.29 / 2 ' sa=0 sb=0 sd=0 mult=2 m=2
XM92 net49 nb VGND VGND sky130_fd_pr__nfet_01v8 L=1 W=2 nf=1 ad='int((1 + 1)/2) * 2 / 1 * 0.29' as='int((1 + 2)/2) * 2 / 1 * 0.29'
+ pd='2*int((1 + 1)/2) * (2 / 1 + 0.29)' ps='2*int((1 + 2)/2) * (2 / 1 + 0.29)' nrd='0.29 / 2 ' nrs='0.29 / 2 '
+ sa=0 sb=0 sd=0 mult=2 m=2
XC1 midp net50 sky130_fd_pr__cap_mim_m3_1 W=22 L=15 MF=1 m=1
XC2 net33 net51 sky130_fd_pr__cap_mim_m3_1 W=12 L=12 MF=1 m=1
XC3 net32 net52 sky130_fd_pr__cap_mim_m3_1 W=12 L=12 MF=1 m=1
XR1 out net50 VGND sky130_fd_pr__res_xhigh_po_1p41 L=2 mult=1 m=1
XR2 net50 net51 VGND sky130_fd_pr__res_xhigh_po_1p41 L=3 mult=1 m=1
XR3 net50 net52 VGND sky130_fd_pr__res_xhigh_po_1p41 L=3 mult=1 m=1
XM94 net33 EN VDPWR VDPWR sky130_fd_pr__pfet_01v8_hvt L=0.15 W=0.42 nf=1 ad='int((1 + 1)/2) * 0.42 / 1 * 0.29'
+ as='int((1 + 2)/2) * 0.42 / 1 * 0.29' pd='2*int((1 + 1)/2) * (0.42 / 1 + 0.29)' ps='2*int((1 + 2)/2) * (0.42 / 1 + 0.29)'
+ nrd='0.29 / 0.42 ' nrs='0.29 / 0.42 ' sa=0 sb=0 sd=0 mult=1 m=1
XM93 net32 EN VDPWR VDPWR sky130_fd_pr__pfet_01v8_hvt L=0.15 W=0.42 nf=1 ad='int((1 + 1)/2) * 0.42 / 1 * 0.29'
+ as='int((1 + 2)/2) * 0.42 / 1 * 0.29' pd='2*int((1 + 1)/2) * (0.42 / 1 + 0.29)' ps='2*int((1 + 2)/2) * (0.42 / 1 + 0.29)'
+ nrd='0.29 / 0.42 ' nrs='0.29 / 0.42 ' sa=0 sb=0 sd=0 mult=1 m=1
XM55d net24 VGND VGND VGND sky130_fd_pr__nfet_01v8 L=1 W=2 nf=1 ad='int((1 + 1)/2) * 2 / 1 * 0.29' as='int((1 + 2)/2) * 2 / 1 * 0.29'
+ pd='2*int((1 + 1)/2) * (2 / 1 + 0.29)' ps='2*int((1 + 2)/2) * (2 / 1 + 0.29)' nrd='0.29 / 2 ' nrs='0.29 / 2 '
+ sa=0 sb=0 sd=0 mult=2 m=2
XM13d net4 VGND VGND VGND sky130_fd_pr__nfet_01v8 L=1 W=2 nf=1 ad='int((1 + 1)/2) * 2 / 1 * 0.29' as='int((1 + 2)/2) * 2 / 1 * 0.29'
+ pd='2*int((1 + 1)/2) * (2 / 1 + 0.29)' ps='2*int((1 + 2)/2) * (2 / 1 + 0.29)' nrd='0.29 / 2 ' nrs='0.29 / 2 '
+ sa=0 sb=0 sd=0 mult=2 m=2
XM51d pinm VDPWR VDPWR VDPWR sky130_fd_pr__pfet_01v8 L=1 W=4 nf=2 ad='int((2 + 1)/2) * 4 / 2 * 0.29'
+ as='int((2 + 2)/2) * 4 / 2 * 0.29' pd='2*int((2 + 1)/2) * (4 / 2 + 0.29)' ps='2*int((2 + 2)/2) * (4 / 2 + 0.29)'
+ nrd='0.29 / 4 ' nrs='0.29 / 4 ' sa=0 sb=0 sd=0 mult=1 m=1
XM54d pinp VDPWR VDPWR VDPWR sky130_fd_pr__pfet_01v8 L=1 W=4 nf=2 ad='int((2 + 1)/2) * 4 / 2 * 0.29'
+ as='int((2 + 2)/2) * 4 / 2 * 0.29' pd='2*int((2 + 1)/2) * (4 / 2 + 0.29)' ps='2*int((2 + 2)/2) * (4 / 2 + 0.29)'
+ nrd='0.29 / 4 ' nrs='0.29 / 4 ' sa=0 sb=0 sd=0 mult=1 m=1
XM40d ninp VGND VGND VGND sky130_fd_pr__nfet_01v8 L=1 W=2 nf=1 ad='int((1 + 1)/2) * 2 / 1 * 0.29' as='int((1 + 2)/2) * 2 / 1 * 0.29'
+ pd='2*int((1 + 1)/2) * (2 / 1 + 0.29)' ps='2*int((1 + 2)/2) * (2 / 1 + 0.29)' nrd='0.29 / 2 ' nrs='0.29 / 2 '
+ sa=0 sb=0 sd=0 mult=2 m=2
**.ends

* expanding   symbol:  /foss/designs/ttsky26c-analog-park/xschem/bias.sym # of pins=5
** sym_path: xschem/bias.sym
** sch_path: xschem/bias.sch
.subckt bias VDPWR pIout VGND EN vbias
*.ipin EN
*.opin pIout
*.ipin VGND
*.ipin VDPWR
*.opin vbias
XM4 inm vbias VDPWR VDPWR sky130_fd_pr__pfet_01v8_lvt L=2 W=2 nf=1 ad='int((1 + 1)/2) * 2 / 1 * 0.29'
+ as='int((1 + 2)/2) * 2 / 1 * 0.29' pd='2*int((1 + 1)/2) * (2 / 1 + 0.29)' ps='2*int((1 + 2)/2) * (2 / 1 + 0.29)'
+ nrd='0.29 / 2 ' nrs='0.29 / 2 ' sa=0 sb=0 sd=0 mult=2 m=2
XM2 inp vbias VDPWR VDPWR sky130_fd_pr__pfet_01v8_lvt L=2 W=2 nf=1 ad='int((1 + 1)/2) * 2 / 1 * 0.29'
+ as='int((1 + 2)/2) * 2 / 1 * 0.29' pd='2*int((1 + 1)/2) * (2 / 1 + 0.29)' ps='2*int((1 + 2)/2) * (2 / 1 + 0.29)'
+ nrd='0.29 / 2 ' nrs='0.29 / 2 ' sa=0 sb=0 sd=0 mult=2 m=2
XM5 pIout vbias VDPWR VDPWR sky130_fd_pr__pfet_01v8_lvt L=2 W=2 nf=1 ad='int((1 + 1)/2) * 2 / 1 * 0.29'
+ as='int((1 + 2)/2) * 2 / 1 * 0.29' pd='2*int((1 + 1)/2) * (2 / 1 + 0.29)' ps='2*int((1 + 2)/2) * (2 / 1 + 0.29)'
+ nrd='0.29 / 2 ' nrs='0.29 / 2 ' sa=0 sb=0 sd=0 mult=2 m=2
XM8 inm inm VGND VGND sky130_fd_pr__nfet_01v8 L=2 W=4 nf=1 ad='int((1 + 1)/2) * 4 / 1 * 0.29' as='int((1 + 2)/2) * 4 / 1 * 0.29'
+ pd='2*int((1 + 1)/2) * (4 / 1 + 0.29)' ps='2*int((1 + 2)/2) * (4 / 1 + 0.29)' nrd='0.29 / 4 ' nrs='0.29 / 4 '
+ sa=0 sb=0 sd=0 mult=1 m=1
XM9 inp inp net1 VGND sky130_fd_pr__nfet_01v8 L=2 W=4 nf=1 ad='int((1 + 1)/2) * 4 / 1 * 0.29' as='int((1 + 2)/2) * 4 / 1 * 0.29'
+ pd='2*int((1 + 1)/2) * (4 / 1 + 0.29)' ps='2*int((1 + 2)/2) * (4 / 1 + 0.29)' nrd='0.29 / 4 ' nrs='0.29 / 4 '
+ sa=0 sb=0 sd=0 mult=4 m=4
XM10 net2 inp VGND VGND sky130_fd_pr__nfet_01v8 L=2 W=2 nf=1 ad='int((1 + 1)/2) * 2 / 1 * 0.29' as='int((1 + 2)/2) * 2 / 1 * 0.29'
+ pd='2*int((1 + 1)/2) * (2 / 1 + 0.29)' ps='2*int((1 + 2)/2) * (2 / 1 + 0.29)' nrd='0.29 / 2 ' nrs='0.29 / 2 '
+ sa=0 sb=0 sd=0 mult=2 m=2
XM11 vbias inm VGND VGND sky130_fd_pr__nfet_01v8 L=2 W=2 nf=1 ad='int((1 + 1)/2) * 2 / 1 * 0.29' as='int((1 + 2)/2) * 2 / 1 * 0.29'
+ pd='2*int((1 + 1)/2) * (2 / 1 + 0.29)' ps='2*int((1 + 2)/2) * (2 / 1 + 0.29)' nrd='0.29 / 2 ' nrs='0.29 / 2 '
+ sa=0 sb=0 sd=0 mult=2 m=2
XM15 vbias startup inm VGND sky130_fd_pr__nfet_01v8_lvt L=0.15 W=0.5 nf=1 ad='int((1 + 1)/2) * 0.5 / 1 * 0.29'
+ as='int((1 + 2)/2) * 0.5 / 1 * 0.29' pd='2*int((1 + 1)/2) * (0.5 / 1 + 0.29)' ps='2*int((1 + 2)/2) * (0.5 / 1 + 0.29)'
+ nrd='0.29 / 0.5 ' nrs='0.29 / 0.5 ' sa=0 sb=0 sd=0 mult=1 m=1
XM3 startup inm VGND VGND sky130_fd_pr__nfet_01v8 L=0.5 W=0.5 nf=1 ad='int((1 + 1)/2) * 0.5 / 1 * 0.29'
+ as='int((1 + 2)/2) * 0.5 / 1 * 0.29' pd='2*int((1 + 1)/2) * (0.5 / 1 + 0.29)' ps='2*int((1 + 2)/2) * (0.5 / 1 + 0.29)'
+ nrd='0.29 / 0.5 ' nrs='0.29 / 0.5 ' sa=0 sb=0 sd=0 mult=1 m=1
XR1 net4 net1 VGND sky130_fd_pr__res_high_po_0p69 L=6.1 mult=1 m=1
XR2 net5 net4 VGND sky130_fd_pr__res_high_po_0p69 L=6.1 mult=1 m=1
XR3 net6 net5 VGND sky130_fd_pr__res_high_po_0p69 L=6.1 mult=1 m=1
XR4 VGND net6 VGND sky130_fd_pr__res_high_po_0p69 L=6.1 mult=1 m=1
XM1 vbias net2 VDPWR VDPWR sky130_fd_pr__pfet_01v8_lvt L=2 W=2 nf=1 ad='int((1 + 1)/2) * 2 / 1 * 0.29'
+ as='int((1 + 2)/2) * 2 / 1 * 0.29' pd='2*int((1 + 1)/2) * (2 / 1 + 0.29)' ps='2*int((1 + 2)/2) * (2 / 1 + 0.29)'
+ nrd='0.29 / 2 ' nrs='0.29 / 2 ' sa=0 sb=0 sd=0 mult=2 m=2
XM12 net2 net2 VDPWR VDPWR sky130_fd_pr__pfet_01v8_lvt L=2 W=2 nf=1 ad='int((1 + 1)/2) * 2 / 1 * 0.29'
+ as='int((1 + 2)/2) * 2 / 1 * 0.29' pd='2*int((1 + 1)/2) * (2 / 1 + 0.29)' ps='2*int((1 + 2)/2) * (2 / 1 + 0.29)'
+ nrd='0.29 / 2 ' nrs='0.29 / 2 ' sa=0 sb=0 sd=0 mult=2 m=2
XM13 startup startup net3 VDPWR sky130_fd_pr__pfet_01v8_lvt L=3 W=0.42 nf=1 ad='int((1 + 1)/2) * 0.42 / 1 * 0.29'
+ as='int((1 + 2)/2) * 0.42 / 1 * 0.29' pd='2*int((1 + 1)/2) * (0.42 / 1 + 0.29)' ps='2*int((1 + 2)/2) * (0.42 / 1 + 0.29)'
+ nrd='0.29 / 0.42 ' nrs='0.29 / 0.42 ' sa=0 sb=0 sd=0 mult=1 m=1
XM16 startup nEN VGND VGND sky130_fd_pr__nfet_01v8 L=0.15 W=0.5 nf=1 ad='int((1 + 1)/2) * 0.5 / 1 * 0.29'
+ as='int((1 + 2)/2) * 0.5 / 1 * 0.29' pd='2*int((1 + 1)/2) * (0.5 / 1 + 0.29)' ps='2*int((1 + 2)/2) * (0.5 / 1 + 0.29)'
+ nrd='0.29 / 0.5 ' nrs='0.29 / 0.5 ' sa=0 sb=0 sd=0 mult=1 m=1
XM17 vbias EN VDPWR VDPWR sky130_fd_pr__pfet_01v8_hvt L=0.15 W=0.42 nf=1 ad='int((1 + 1)/2) * 0.42 / 1 * 0.29'
+ as='int((1 + 2)/2) * 0.42 / 1 * 0.29' pd='2*int((1 + 1)/2) * (0.42 / 1 + 0.29)' ps='2*int((1 + 2)/2) * (0.42 / 1 + 0.29)'
+ nrd='0.29 / 0.42 ' nrs='0.29 / 0.42 ' sa=0 sb=0 sd=0 mult=1 m=1
XM7 net3 nEN VDPWR VDPWR sky130_fd_pr__pfet_01v8_hvt L=0.15 W=0.42 nf=1 ad='int((1 + 1)/2) * 0.42 / 1 * 0.29'
+ as='int((1 + 2)/2) * 0.42 / 1 * 0.29' pd='2*int((1 + 1)/2) * (0.42 / 1 + 0.29)' ps='2*int((1 + 2)/2) * (0.42 / 1 + 0.29)'
+ nrd='0.29 / 0.42 ' nrs='0.29 / 0.42 ' sa=0 sb=0 sd=0 mult=1 m=1
XM14 VDPWR vbias VDPWR VDPWR sky130_fd_pr__pfet_01v8_lvt L=3 W=4 nf=1 ad='int((1 + 1)/2) * 4 / 1 * 0.29'
+ as='int((1 + 2)/2) * 4 / 1 * 0.29' pd='2*int((1 + 1)/2) * (4 / 1 + 0.29)' ps='2*int((1 + 2)/2) * (4 / 1 + 0.29)'
+ nrd='0.29 / 4 ' nrs='0.29 / 4 ' sa=0 sb=0 sd=0 mult=6 m=6
x1 EN VGND VGND VDPWR VDPWR nEN sky130_fd_sc_hd__inv_1
.ends

.end
